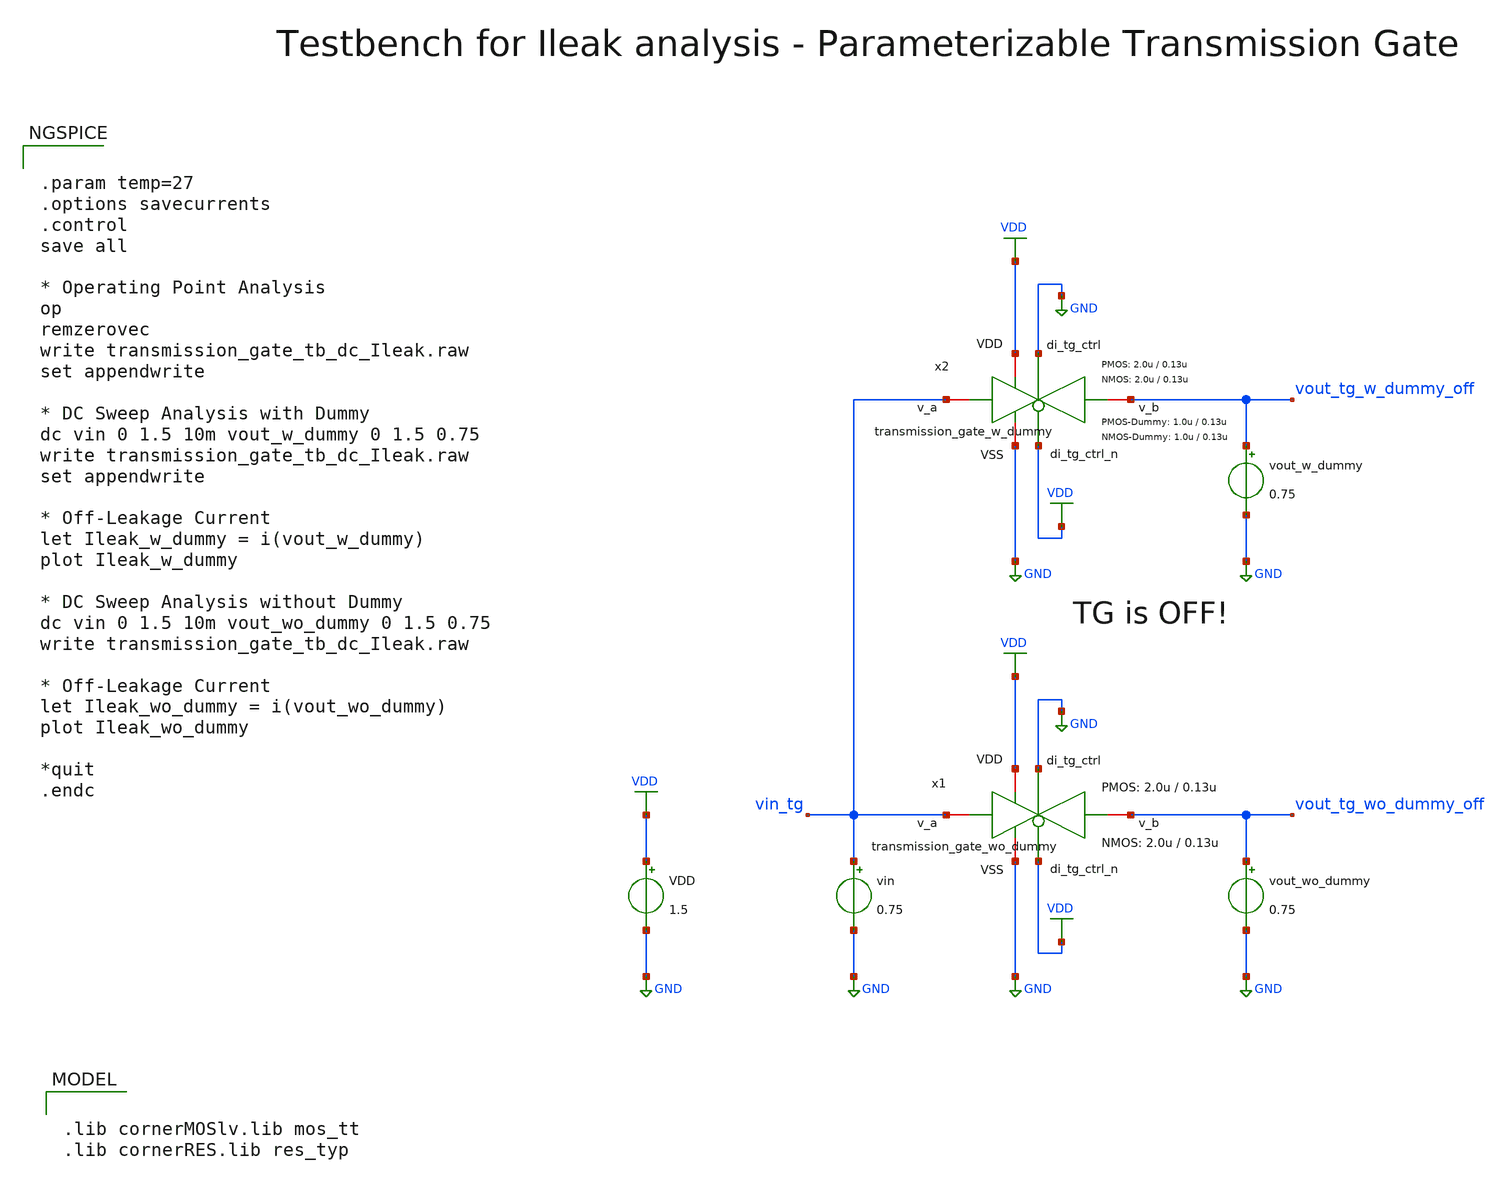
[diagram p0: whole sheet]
** sch_path: xschem/transmission_gate/testbenches/transmission_gate_tb_dc_Ileak.sch
**.subckt transmission_gate_tb_dc_Ileak
VDD VDD GND 1.5
vin vin_tg GND 0.75
vout_wo_dummy vout_tg_wo_dummy_off GND 0.75
x1 VDD GND GND vout_tg_wo_dummy_off vin_tg VDD transmission_gate_wo_dummy W_P=2.0u L_P=0.13u
+ W_N=2.0u L_N=0.13u
x2 VDD GND GND vout_tg_w_dummy_off vin_tg VDD transmission_gate_w_dummy W_P=2.0u L_P=0.13u W_N=2.0u
+ L_N=0.13u W_P_D=1.0u L_P_D=0.13u W_N_D=1.0u L_N_D=0.13u
vout_w_dummy vout_tg_w_dummy_off GND 0.75
**** begin user architecture code

.lib cornerMOSlv.lib mos_tt
.lib cornerRES.lib res_typ



.param temp=27
.options savecurrents
.control
save all

* Operating Point Analysis
op
remzerovec
write transmission_gate_tb_dc_Ileak.raw
set appendwrite

* DC Sweep Analysis with Dummy
dc vin 0 1.5 10m vout_w_dummy 0 1.5 0.75
write transmission_gate_tb_dc_Ileak.raw
set appendwrite

* Off-Leakage Current
let Ileak_w_dummy = i(vout_w_dummy)
plot Ileak_w_dummy

* DC Sweep Analysis without Dummy
dc vin 0 1.5 10m vout_wo_dummy 0 1.5 0.75
write transmission_gate_tb_dc_Ileak.raw

* Off-Leakage Current
let Ileak_wo_dummy = i(vout_wo_dummy)
plot Ileak_wo_dummy

*quit
.endc

**** end user architecture code
**.ends

* expanding   symbol:  transmission_gate/transmission_gate_wo_dummy.sym # of pins=6
** sym_path: xschem/transmission_gate/transmission_gate_wo_dummy.sym
** sch_path: xschem/transmission_gate/transmission_gate_wo_dummy.sch
.subckt transmission_gate_wo_dummy VDD di_tg_ctrl VSS v_b v_a di_tg_ctrl_n  W_P=3.0u L_P=0.13u
+ W_N=1.0u L_N=0.13u
*.iopin v_a
*.iopin v_b
*.iopin VDD
*.iopin VSS
*.ipin di_tg_ctrl
*.ipin di_tg_ctrl_n
XM1 v_b di_tg_ctrl v_a VSS sg13_lv_nmos w=W_N l=L_N ng=1 m=1 mm_ok=1
XM2 v_a di_tg_ctrl_n v_b VDD sg13_lv_pmos w=W_P l=L_P ng=1 m=1 mm_ok=1
.ends


* expanding   symbol:  transmission_gate/transmission_gate_w_dummy.sym # of pins=6
** sym_path: xschem/transmission_gate/transmission_gate_w_dummy.sym
** sch_path: xschem/transmission_gate/transmission_gate_w_dummy.sch
.subckt transmission_gate_w_dummy VDD di_tg_ctrl VSS v_b v_a di_tg_ctrl_n  W_P=2.0u L_P=0.13u
+ W_N=2.0u L_N=0.13u W_P_D=1.0u L_P_D=0.13u W_N_D=1.0u L_N_D=0.13u
*.iopin v_a
*.iopin v_b
*.iopin VDD
*.iopin VSS
*.ipin di_tg_ctrl
*.ipin di_tg_ctrl_n
XM1 v_b di_tg_ctrl v_a VSS sg13_lv_nmos w=W_N l=L_N ng=1 m=1 mm_ok=1
XM2 v_a di_tg_ctrl_n v_b VDD sg13_lv_pmos w=W_P l=L_P ng=1 m=1 mm_ok=1
XMdummy2 v_b di_tg_ctrl v_b VDD sg13_lv_pmos w=W_P_D l=L_P_D ng=1 m=1 mm_ok=1
XMdummy1 v_b di_tg_ctrl_n v_b VSS sg13_lv_nmos w=W_N_D l=L_N_D ng=1 m=1 mm_ok=1
.ends

.GLOBAL GND
.GLOBAL VDD
.end
